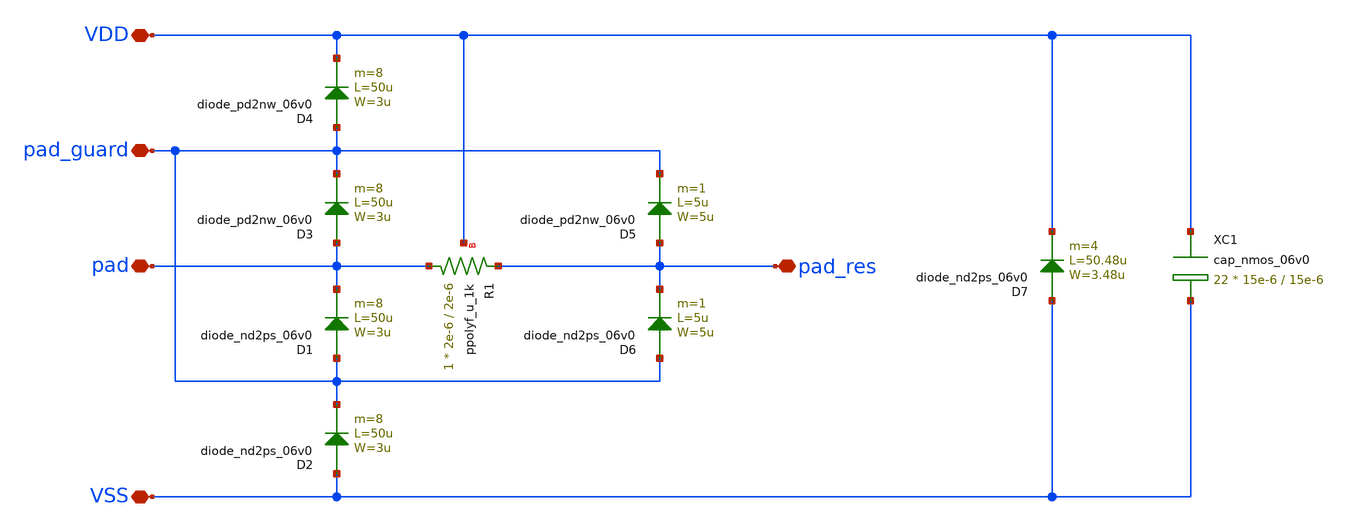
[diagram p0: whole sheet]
** sch_path: xschem/gf180mcu_fd_io__asig_guard_5p0_70x100.sch
**.subckt gf180mcu_fd_io__asig_guard_5p0_70x100 pad pad_guard VDD VSS pad_res
*.iopin pad
*.iopin pad_guard
*.iopin VDD
*.iopin VSS
*.iopin pad_res
D1 pad_guard pad diode_nd2ps_06v0 area='3u * 50u ' pj='2*3u + 2*50u ' m=8
D2 VSS pad_guard diode_nd2ps_06v0 area='3u * 50u ' pj='2*3u + 2*50u ' m=8
D3 pad pad_guard diode_pd2nw_06v0 area='3u * 50u ' pj='2*3u + 2*50u ' m=8
D4 pad_guard VDD diode_pd2nw_06v0 area='3u * 50u ' pj='2*3u + 2*50u ' m=8
XR1 pad pad_res VDD ppolyf_u_1k r_width=2e-6 r_length=2e-6 m=1
D5 pad_res pad_guard diode_pd2nw_06v0 area='5u * 5u ' pj='2*5u + 2*5u ' m=1
D6 pad_guard pad_res diode_nd2ps_06v0 area='5u * 5u ' pj='2*5u + 2*5u ' m=1
D7 VSS VDD diode_nd2ps_06v0 area='3.48u * 50.48u ' pj='2*3.48u + 2*50.48u ' m=4
XC1 VDD VSS cap_nmos_06v0 c_width=15e-6 c_length=15e-6 m=22
**.ends
.end
